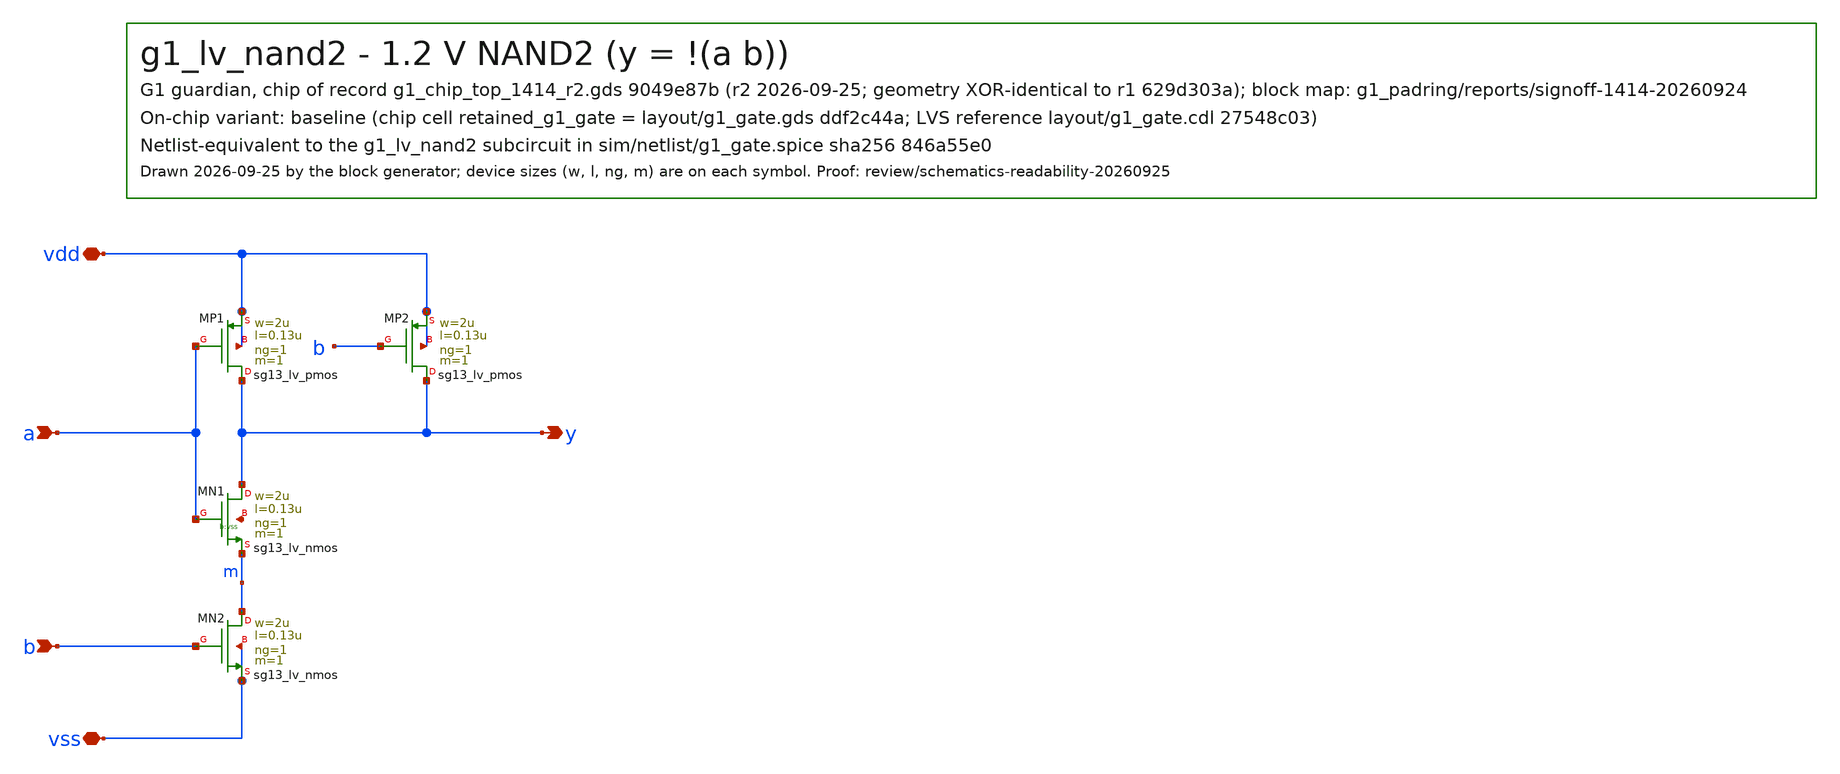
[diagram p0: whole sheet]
** sch_path: designs/g1-guardian/blocks/g1_gate/schematic/g1_lv_nand2.sch
**.subckt g1_lv_nand2 a b y vdd vss
*.ipin a
*.ipin b
*.opin y
*.iopin vdd
*.iopin vss
XMP1 y a vdd vdd sg13_lv_pmos w=2u l=0.13u ng=1 m=1 mm_ok=1
XMP2 y b vdd vdd sg13_lv_pmos w=2u l=0.13u ng=1 m=1 mm_ok=1
XMN1 y a m vss sg13_lv_nmos w=2u l=0.13u ng=1 m=1 mm_ok=1
XMN2 m b vss vss sg13_lv_nmos w=2u l=0.13u ng=1 m=1 mm_ok=1
**.ends
.end
